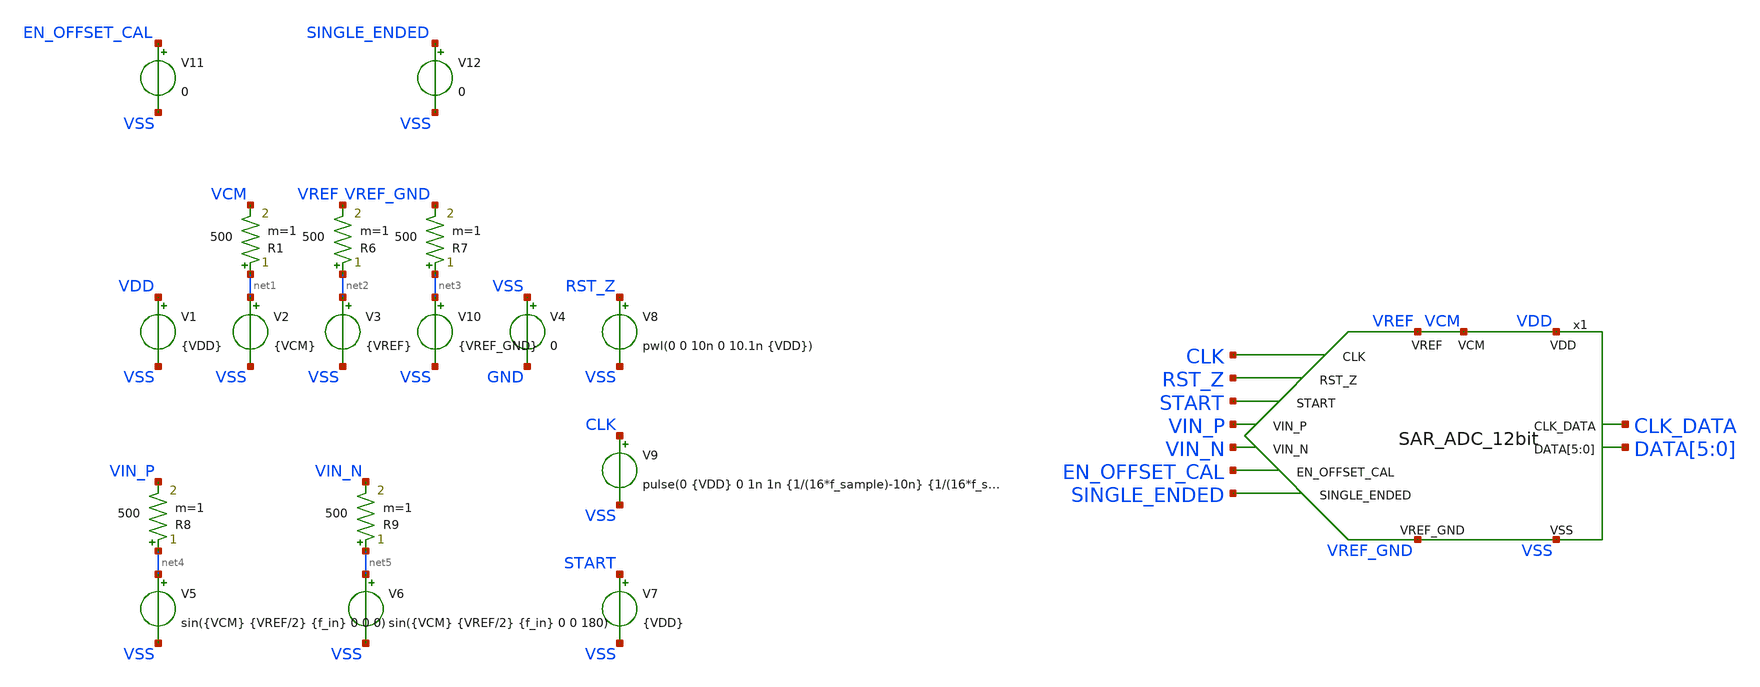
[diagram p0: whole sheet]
** sch_path: Schematic/top_tb.sch
**.subckt top_tb
x1 VDD VCM VSS VREF VIN_P VIN_N RST_Z CLK_DATA DATA[5] DATA[4] DATA[3] DATA[2] DATA[1] DATA[0] START
+ EN_OFFSET_CAL CLK VREF_GND SINGLE_ENDED SAR_ADC_12bit
V1 VDD VSS {VDD}
.save i(v1)
V2 net1 VSS {VCM}
.save i(v2)
V3 net2 VSS {VREF}
.save i(v3)
V4 VSS GND 0
V7 START VSS {VDD}
V8 RST_Z VSS pwl(0 0 10n 0 10.1n {VDD})
V5 net4 VSS sin({VCM} {VREF/2} {f_in} 0 0 0)
R1 net1 VCM 500 m=1
V9 CLK VSS pulse(0 {VDD} 0 1n 1n {1/(16*f_sample)-10n} {1/(16*f_sample)})
V6 net5 VSS sin({VCM} {VREF/2} {f_in} 0 0 180)
V10 net3 VSS {VREF_GND}
.save i(v10)
R6 net2 VREF 500 m=1
R7 net3 VREF_GND 500 m=1
R8 net4 VIN_P 500 m=1
R9 net5 VIN_N 500 m=1
V11 EN_OFFSET_CAL VSS 0
V12 SINGLE_ENDED VSS 0
**** begin user architecture code


* Supply, common mode and reference voltage
.param VDD = 1.8
.param VREF = 1.2
.param VREF_GND = 0
.param VCM = 0.6

.option temp = 27

* Input and sampling frequencies
* For coherent sampling f_in is calculated
.param n_window = 67
.param n_fft = 256
.param f_sample = 1.25Meg
.param f_in = {f_sample*n_window/n_fft}

*.save all

* Control signals
.save start rst_z clk en_offset_cal

* Input signals
.save vin_p vin_n

* Reference, supply
.save vref vref_gnd vcm vdd

* Output signals
.save clk_data data[5] data[4] data[3] data[2] data[1] data[0]

* Internal signals
.save x1.vdac_p x1.vdac_n x1.vdac_pi x1.vdac_ni x1.smpl x1.en_comp x1.comp_p x1.comp_n x1.cal_p x1.cal_n
.save x1.en_vin_bstr_p x1.en_vin_bstr_n
*.save x1.c10_p_btm x1.c9_p_btm x1.c8_p_btm x1.c7_p_btm x1.c6_p_btm x1.c5_p_btm x1.c4_p_btm x1.c3_p_btm x1.c2_p_btm x1.c1_p_btm x1.c0_p_btm x1.C0_dummy_p_btm
*.save x1.c10_n_btm x1.c9_n_btm x1.c8_n_btm x1.c7_n_btm x1.c6_n_btm x1.c5_n_btm x1.c4_n_btm x1.c3_n_btm x1.c2_n_btm x1.c1_n_btm x1.c0_n_btm x1.C0_dummy_n_btm

.option GMIN=1e-12 reltol=1e-5
.control
		set ngbehavior=hsa
          		*set skywaterpdk
          		set ng_nomodcheck
          		set num_threads=4
          		option noinit
          		option klu
		* stop time = (n_fft+4)/f_sample
		tran 10n 208u
		write top_level_enob_sim.raw
.endc



.include $::180MCU_MODELS/design.ngspice
.lib $::180MCU_MODELS/sm141064.ngspice typical
.lib $::180MCU_MODELS/sm141064.ngspice cap_mim
.lib $::180MCU_MODELS/sm141064.ngspice res_typical
.lib $::180MCU_MODELS/sm141064.ngspice moscap_typical
.lib $::180MCU_MODELS/sm141064.ngspice mimcap_typical
.lib $::180MCU_MODELS/sm141064.ngspice res_statistical
.lib $::180MCU_MODELS/smbb000149.ngspice typical





* Models for standard digital cells

.include ~/conda-gf180mcu-env/envs/gf180mcu-env/share/pdk/gf180mcuD/libs.ref/gf180mcu_fd_sc_mcu7t5v0/spice/gf180mcu_fd_sc_mcu7t5v0.spice


* Spice netlist for state machine generated by openlane
.include ~/Sar_ADC_12bit/Schematic/state_machine/openlane/runs/gf_run5/results/signoff/state_machine.spice




**** end user architecture code
**.ends
.end
